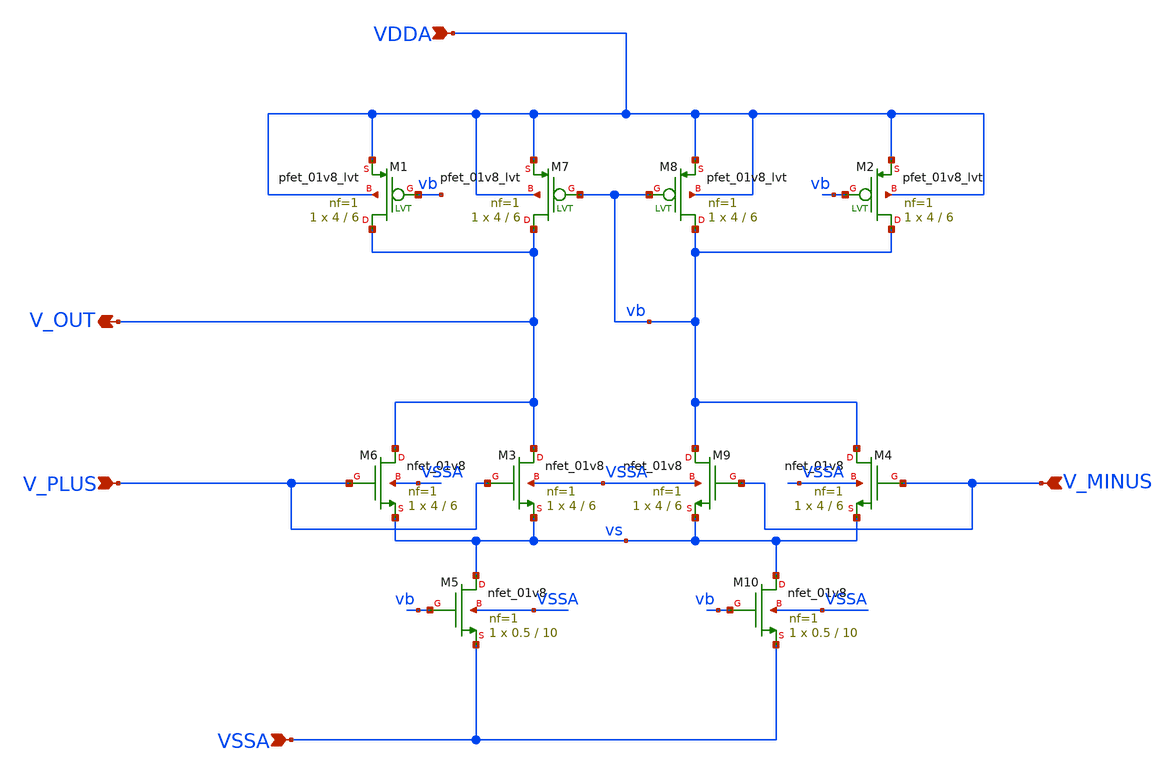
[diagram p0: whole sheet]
** sch_path: lef/bg2_opamp.sch
**.subckt bg2_opamp VDDA VSSA V_PLUS V_MINUS V_OUT
*.ipin VDDA
*.ipin VSSA
*.ipin V_PLUS
*.ipin V_MINUS
*.opin V_OUT
XM3 V_OUT V_PLUS vs VSSA sky130_fd_pr__nfet_01v8 L=6 W=4 nf=1 ad='int((1 + 1)/2) * 4 / 1 * 0.29' as='int((1 + 2)/2) * 4 / 1 * 0.29'
+ pd='2*int((1 + 1)/2) * (4 / 1 + 0.29)' ps='2*int((1 + 2)/2) * (4 / 1 + 0.29)' nrd='0.29 / 4 ' nrs='0.29 / 4 '
+ sa=0 sb=0 sd=0 mult=1 m=1
XM7 V_OUT vb VDDA VDDA sky130_fd_pr__pfet_01v8_lvt L=6 W=4 nf=1 ad='int((1 + 1)/2) * 4 / 1 * 0.29' as='int((1 + 2)/2) * 4 / 1 * 0.29'
+ pd='2*int((1 + 1)/2) * (4 / 1 + 0.29)' ps='2*int((1 + 2)/2) * (4 / 1 + 0.29)' nrd='0.29 / 4 ' nrs='0.29 / 4 '
+ sa=0 sb=0 sd=0 mult=1 m=1
XM8 vb vb VDDA VDDA sky130_fd_pr__pfet_01v8_lvt L=6 W=4 nf=1 ad='int((1 + 1)/2) * 4 / 1 * 0.29' as='int((1 + 2)/2) * 4 / 1 * 0.29'
+ pd='2*int((1 + 1)/2) * (4 / 1 + 0.29)' ps='2*int((1 + 2)/2) * (4 / 1 + 0.29)' nrd='0.29 / 4 ' nrs='0.29 / 4 '
+ sa=0 sb=0 sd=0 mult=1 m=1
XM9 vb V_MINUS vs VSSA sky130_fd_pr__nfet_01v8 L=6 W=4 nf=1 ad='int((1 + 1)/2) * 4 / 1 * 0.29' as='int((1 + 2)/2) * 4 / 1 * 0.29'
+ pd='2*int((1 + 1)/2) * (4 / 1 + 0.29)' ps='2*int((1 + 2)/2) * (4 / 1 + 0.29)' nrd='0.29 / 4 ' nrs='0.29 / 4 '
+ sa=0 sb=0 sd=0 mult=1 m=1
XM10 vs vb VSSA VSSA sky130_fd_pr__nfet_01v8 L=10 W=0.5 nf=1 ad='int((1 + 1)/2) * 0.5 / 1 * 0.29' as='int((1 + 2)/2) * 0.5 / 1 * 0.29'
+ pd='2*int((1 + 1)/2) * (0.5 / 1 + 0.29)' ps='2*int((1 + 2)/2) * (0.5 / 1 + 0.29)' nrd='0.29 / 0.5 ' nrs='0.29 / 0.5 '
+ sa=0 sb=0 sd=0 mult=1 m=1
XM1 V_OUT vb VDDA VDDA sky130_fd_pr__pfet_01v8_lvt L=6 W=4 nf=1 ad='int((1 + 1)/2) * 4 / 1 * 0.29' as='int((1 + 2)/2) * 4 / 1 * 0.29'
+ pd='2*int((1 + 1)/2) * (4 / 1 + 0.29)' ps='2*int((1 + 2)/2) * (4 / 1 + 0.29)' nrd='0.29 / 4 ' nrs='0.29 / 4 '
+ sa=0 sb=0 sd=0 mult=1 m=1
XM2 vb vb VDDA VDDA sky130_fd_pr__pfet_01v8_lvt L=6 W=4 nf=1 ad='int((1 + 1)/2) * 4 / 1 * 0.29' as='int((1 + 2)/2) * 4 / 1 * 0.29'
+ pd='2*int((1 + 1)/2) * (4 / 1 + 0.29)' ps='2*int((1 + 2)/2) * (4 / 1 + 0.29)' nrd='0.29 / 4 ' nrs='0.29 / 4 '
+ sa=0 sb=0 sd=0 mult=1 m=1
XM6 V_OUT V_PLUS vs VSSA sky130_fd_pr__nfet_01v8 L=6 W=4 nf=1 ad='int((1 + 1)/2) * 4 / 1 * 0.29' as='int((1 + 2)/2) * 4 / 1 * 0.29'
+ pd='2*int((1 + 1)/2) * (4 / 1 + 0.29)' ps='2*int((1 + 2)/2) * (4 / 1 + 0.29)' nrd='0.29 / 4 ' nrs='0.29 / 4 '
+ sa=0 sb=0 sd=0 mult=1 m=1
XM4 vb V_MINUS vs VSSA sky130_fd_pr__nfet_01v8 L=6 W=4 nf=1 ad='int((1 + 1)/2) * 4 / 1 * 0.29' as='int((1 + 2)/2) * 4 / 1 * 0.29'
+ pd='2*int((1 + 1)/2) * (4 / 1 + 0.29)' ps='2*int((1 + 2)/2) * (4 / 1 + 0.29)' nrd='0.29 / 4 ' nrs='0.29 / 4 '
+ sa=0 sb=0 sd=0 mult=1 m=1
XM5 vs vb VSSA VSSA sky130_fd_pr__nfet_01v8 L=10 W=0.5 nf=1 ad='int((1 + 1)/2) * 0.5 / 1 * 0.29' as='int((1 + 2)/2) * 0.5 / 1 * 0.29'
+ pd='2*int((1 + 1)/2) * (0.5 / 1 + 0.29)' ps='2*int((1 + 2)/2) * (0.5 / 1 + 0.29)' nrd='0.29 / 0.5 ' nrs='0.29 / 0.5 '
+ sa=0 sb=0 sd=0 mult=1 m=1
**.ends
.end
